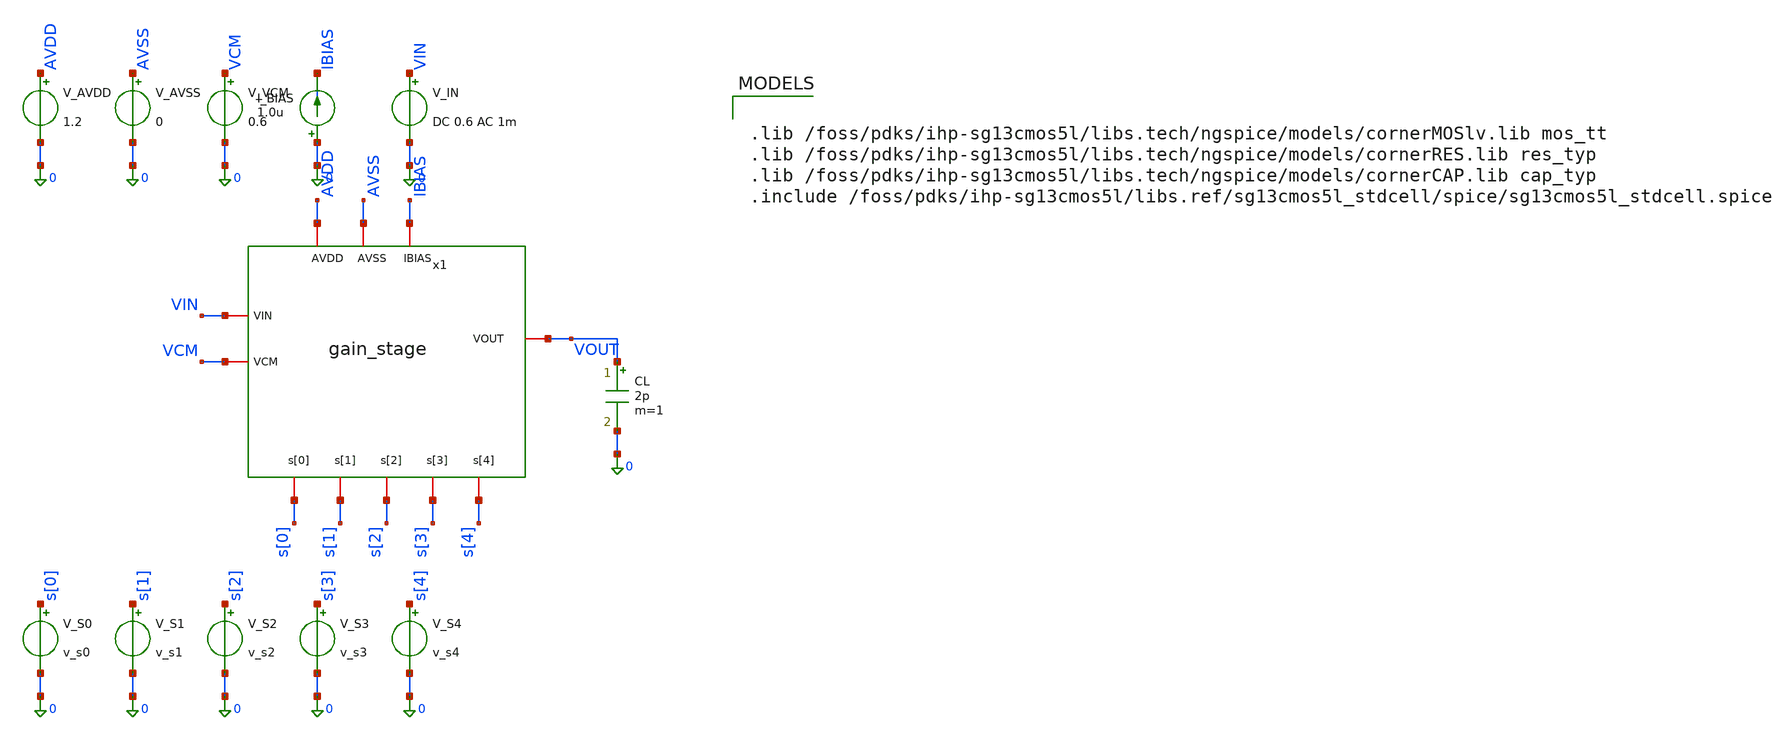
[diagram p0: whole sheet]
** sch_path: xschem/gain_stage/tb_gain_stage.sch
**.subckt tb_gain_stage
x1 AVDD AVSS IBIAS VIN VCM VOUT s[0] s[1] s[2] s[3] s[4] gain_stage
V_AVDD AVDD 0 1.2
V_AVSS AVSS 0 0
V_VCM VCM 0 0.6
I_BIAS 0 IBIAS 1.0u
V_IN VIN 0 DC 0.6 AC 1m
CL VOUT 0 2p m=1
V_S0 s[0] 0 v_s0
V_S1 s[1] 0 v_s1
V_S2 s[2] 0 v_s2
V_S3 s[3] 0 v_s3
V_S4 s[4] 0 v_s4
**** begin user architecture code


.lib /foss/pdks/ihp-sg13cmos5l/libs.tech/ngspice/models/cornerMOSlv.lib mos_tt
.lib /foss/pdks/ihp-sg13cmos5l/libs.tech/ngspice/models/cornerRES.lib res_typ
.lib /foss/pdks/ihp-sg13cmos5l/libs.tech/ngspice/models/cornerCAP.lib cap_typ
.include /foss/pdks/ihp-sg13cmos5l/libs.ref/sg13cmos5l_stdcell/spice/sg13cmos5l_stdcell.spice




.param v_s0=0 v_s1=0 v_s2=0 v_s3=0 v_s4=0

.control
  save all
  echo ==========================================================================
  echo === GAIN STAGE TAP CHARACTERIZATION (VERIFYING STANDARD CELL S0 LOGIC) ===
  echo ==========================================================================

  * Tap 0: s = 00000 (Target: 0.0 dB / 1x)
  alterparam v_s0=0
  alterparam v_s1=0
  alterparam v_s2=0
  alterparam v_s3=0
  alterparam v_s4=0
  reset
  op
  let s0_dc0 = v(x1.S0)
  ac dec 10 1k 100Meg
  let gain0 = db(v(VOUT)/v(VIN))
  let g0_val = gain0[10]
  echo Tap 0 (s=00000): S0 DC = $&s0_dc0 V | AC Gain @ 10kHz = $&g0_val dB (Target: 0.00 dB)

  * Tap 1: s = 00001 (Target: 6.02 dB / 2x)
  alterparam v_s0=1.2
  alterparam v_s1=0
  alterparam v_s2=0
  alterparam v_s3=0
  alterparam v_s4=0
  reset
  op
  let s0_dc1 = v(x1.S0)
  ac dec 10 1k 100Meg
  let gain1 = db(v(VOUT)/v(VIN))
  let g1_val = gain1[10]
  echo Tap 1 (s=00001): S0 DC = $&s0_dc1 V | AC Gain @ 10kHz = $&g1_val dB (Target: 6.02 dB)

  * Tap 2: s = 00010 (Target: 12.04 dB / 4x)
  alterparam v_s0=0
  alterparam v_s1=1.2
  alterparam v_s2=0
  alterparam v_s3=0
  alterparam v_s4=0
  reset
  op
  let s0_dc2 = v(x1.S0)
  ac dec 10 1k 100Meg
  let gain2 = db(v(VOUT)/v(VIN))
  let g2_val = gain2[10]
  echo Tap 2 (s=00010): S0 DC = $&s0_dc2 V | AC Gain @ 10kHz = $&g2_val dB (Target: 12.04 dB)

  * Tap 3: s = 00100 (Target: 18.06 dB / 8x)
  alterparam v_s0=0
  alterparam v_s1=0
  alterparam v_s2=1.2
  alterparam v_s3=0
  alterparam v_s4=0
  reset
  op
  let s0_dc3 = v(x1.S0)
  ac dec 10 1k 100Meg
  let gain3 = db(v(VOUT)/v(VIN))
  let g3_val = gain3[10]
  echo Tap 3 (s=00100): S0 DC = $&s0_dc3 V | AC Gain @ 10kHz = $&g3_val dB (Target: 18.06 dB)

  * Tap 4: s = 01000 (Target: 24.08 dB / 16x)
  alterparam v_s0=0
  alterparam v_s1=0
  alterparam v_s2=0
  alterparam v_s3=1.2
  alterparam v_s4=0
  reset
  op
  let s0_dc4 = v(x1.S0)
  ac dec 10 1k 100Meg
  let gain4 = db(v(VOUT)/v(VIN))
  let g4_val = gain4[10]
  echo Tap 4 (s=01000): S0 DC = $&s0_dc4 V | AC Gain @ 10kHz = $&g4_val dB (Target: 24.08 dB)

  * Tap 5: s = 10000 (Target: 30.10 dB / 32x)
  alterparam v_s0=0
  alterparam v_s1=0
  alterparam v_s2=0
  alterparam v_s3=0
  alterparam v_s4=1.2
  reset
  op
  let s0_dc5 = v(x1.S0)
  ac dec 10 1k 100Meg
  let gain5 = db(v(VOUT)/v(VIN))
  let g5_val = gain5[10]
  echo Tap 5 (s=10000): S0 DC = $&s0_dc5 V | AC Gain @ 10kHz = $&g5_val dB (Target: 30.10 dB)

  echo ==========================================================================
  echo === CHARACTERIZATION COMPLETE ===
  echo ==========================================================================
.endc


**** end user architecture code
**.ends
.end
